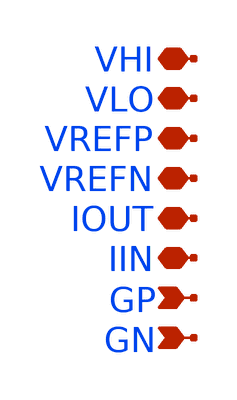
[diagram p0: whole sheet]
** sch_path: xschem/isrc_PEX.sch
**.subckt isrc_PEX VHI VLO VREFP IOUT VREFN IIN GP GN
*.iopin VHI
*.iopin VLO
*.iopin VREFP
*.iopin IOUT
*.iopin VREFN
*.iopin IIN
*.ipin GP
*.ipin GN
**** begin user architecture code

.subckt isrc VHI VLO IIN IOUT GN GP VREFP VREFN

X1 VHI GN IN VHI sky130_fd_pr__pfet_01v8 ad=0p pd=0u as=0p ps=0u w=1e+07u l=150000u
X2 VHI VHI VREFP VHI sky130_fd_pr__pfet_01v8 ad=0p pd=0u as=0p ps=0u w=1e+07u l=2e+06u
X3 VLO GP IP VLO sky130_fd_pr__nfet_01v8 ad=0p pd=0u as=0p ps=0u w=5e+06u l=150000u
X4 VLO VLO a_314_3386# VLO sky130_fd_pr__nfet_01v8 ad=0p pd=0u as=0p ps=0u w=5e+06u l=2e+06u
X5 a_314_3386# VREFP VLO sky130_fd_pr__res_xhigh_po w=350000u l=5.17e+06u
X7 VLO VLO VREFN VLO sky130_fd_pr__nfet_01v8 ad=0p pd=0u as=0p ps=0u w=5e+06u l=2e+06u
X8 IP VREFP VHI VHI sky130_fd_pr__pfet_01v8 ad=0p pd=0u as=0p ps=0u w=1e+07u l=2e+06u
X9 IN VREFN VLO VLO sky130_fd_pr__nfet_01v8 ad=0p pd=0u as=0p ps=0u w=5e+06u l=2e+06u
X10 IOUT GP IP VHI sky130_fd_pr__pfet_01v8 ad=0p pd=0u as=0p ps=0u w=1e+07u l=150000u
X11 VHI VHI IP VHI sky130_fd_pr__pfet_01v8 ad=0p pd=0u as=0p ps=0u w=1e+07u l=2e+06u
X12 VREFN VREFN VLO VLO sky130_fd_pr__nfet_01v8 ad=0p pd=0u as=0p ps=0u w=5e+06u l=2e+06u
X13 IOUT GN IN VLO sky130_fd_pr__nfet_01v8 ad=0p pd=0u as=0p ps=0u w=5e+06u l=150000u
X14 VLO VLO IN VLO sky130_fd_pr__nfet_01v8 ad=0p pd=0u as=0p ps=0u w=5e+06u l=2e+06u
X15 VREFP VREFP VHI VHI sky130_fd_pr__pfet_01v8 ad=0p pd=0u as=0p ps=0u w=1e+07u l=2e+06u
X16 a_314_3386# VREFN VLO VLO sky130_fd_pr__nfet_01v8 ad=0p pd=0u as=0p ps=0u w=5e+06u l=2e+06u
C0 VHI IN 2.47fF
C1 IOUT IP 2.22fF
C2 VHI IP 3.75fF
C3 VHI VREFP 6.31fF
C4 VREFN VLO 7.88fF $ **FLOATING
C5 IN VLO 2.16fF $ **FLOATING
C6 a_314_3386# VLO 2.09fF $ **FLOATING
C7 VHI VLO 30.82fF $ **FLOATING

.ends


XDUT VHI VLO IIN IOUT GN GP VREFP VREFN isrc


**** end user architecture code
**.ends
.end
